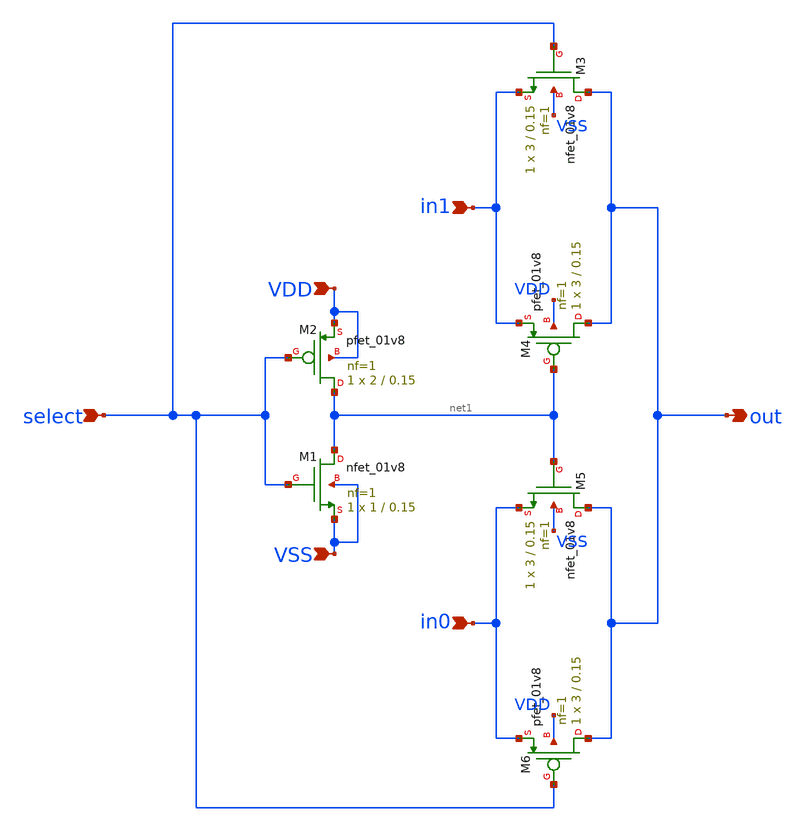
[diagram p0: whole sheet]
** sch_path: MUX_2to1.sch
**.subckt MUX_2to1 select VSS VDD in1 in0 out
*.ipin select
*.ipin VSS
*.ipin VDD
*.ipin in1
*.ipin in0
*.opin out
XM1 net1 select VSS VSS sky130_fd_pr__nfet_01v8 L=0.15 W=1 nf=1 ad='int((nf+1)/2) * W/nf * 0.29' as='int((nf+2)/2) * W/nf * 0.29'
+ pd='2*int((nf+1)/2) * (W/nf + 0.29)' ps='2*int((nf+2)/2) * (W/nf + 0.29)' nrd='0.29 / W' nrs='0.29 / W'
+ sa=0 sb=0 sd=0 mult=1 m=1
XM2 net1 select VDD VDD sky130_fd_pr__pfet_01v8 L=0.15 W=2 nf=1 ad='int((nf+1)/2) * W/nf * 0.29' as='int((nf+2)/2) * W/nf * 0.29'
+ pd='2*int((nf+1)/2) * (W/nf + 0.29)' ps='2*int((nf+2)/2) * (W/nf + 0.29)' nrd='0.29 / W' nrs='0.29 / W'
+ sa=0 sb=0 sd=0 mult=1 m=1
XM3 out select in1 VSS sky130_fd_pr__nfet_01v8 L=0.15 W=3 nf=1 ad='int((nf+1)/2) * W/nf * 0.29' as='int((nf+2)/2) * W/nf * 0.29'
+ pd='2*int((nf+1)/2) * (W/nf + 0.29)' ps='2*int((nf+2)/2) * (W/nf + 0.29)' nrd='0.29 / W' nrs='0.29 / W'
+ sa=0 sb=0 sd=0 mult=1 m=1
XM4 out net1 in1 VDD sky130_fd_pr__pfet_01v8 L=0.15 W=3 nf=1 ad='int((nf+1)/2) * W/nf * 0.29' as='int((nf+2)/2) * W/nf * 0.29'
+ pd='2*int((nf+1)/2) * (W/nf + 0.29)' ps='2*int((nf+2)/2) * (W/nf + 0.29)' nrd='0.29 / W' nrs='0.29 / W'
+ sa=0 sb=0 sd=0 mult=1 m=1
XM5 out net1 in0 VSS sky130_fd_pr__nfet_01v8 L=0.15 W=3 nf=1 ad='int((nf+1)/2) * W/nf * 0.29' as='int((nf+2)/2) * W/nf * 0.29'
+ pd='2*int((nf+1)/2) * (W/nf + 0.29)' ps='2*int((nf+2)/2) * (W/nf + 0.29)' nrd='0.29 / W' nrs='0.29 / W'
+ sa=0 sb=0 sd=0 mult=1 m=1
XM6 out select in0 VDD sky130_fd_pr__pfet_01v8 L=0.15 W=3 nf=1 ad='int((nf+1)/2) * W/nf * 0.29' as='int((nf+2)/2) * W/nf * 0.29'
+ pd='2*int((nf+1)/2) * (W/nf + 0.29)' ps='2*int((nf+2)/2) * (W/nf + 0.29)' nrd='0.29 / W' nrs='0.29 / W'
+ sa=0 sb=0 sd=0 mult=1 m=1
**.ends
.end
